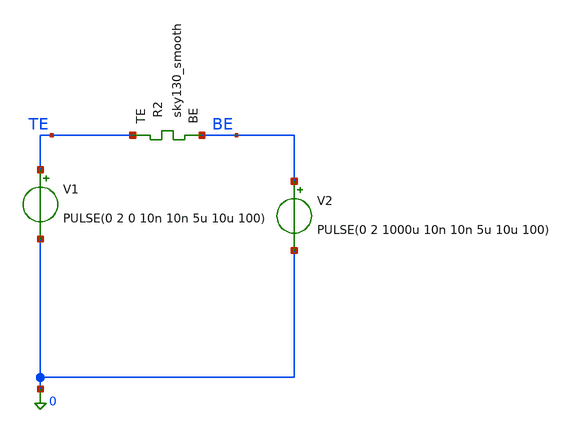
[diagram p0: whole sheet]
** sch_path: memristor_models/sky130_smooth/tb_1R_smooth.sch
**.subckt tb_1R_smooth
V1 TE 0 PULSE(0 2 0 10n 10n 5u 10u 100)
XR2 TE BE sky130_smooth Tfilament_0=3.3e-9
V2 BE 0 PULSE(0 2 1000u 10n 10n 5u 10u 100)
**** begin user architecture code

** opencircuitdesign pdks install
.inc $::SKYWATER_MODELS/sky130_smooth.spice



.option savecurrents
.tran 1u 3000u
.control
	save all
	run
	write tb_1R_smooth.raw
.endc



**** end user architecture code
**.ends
.end
